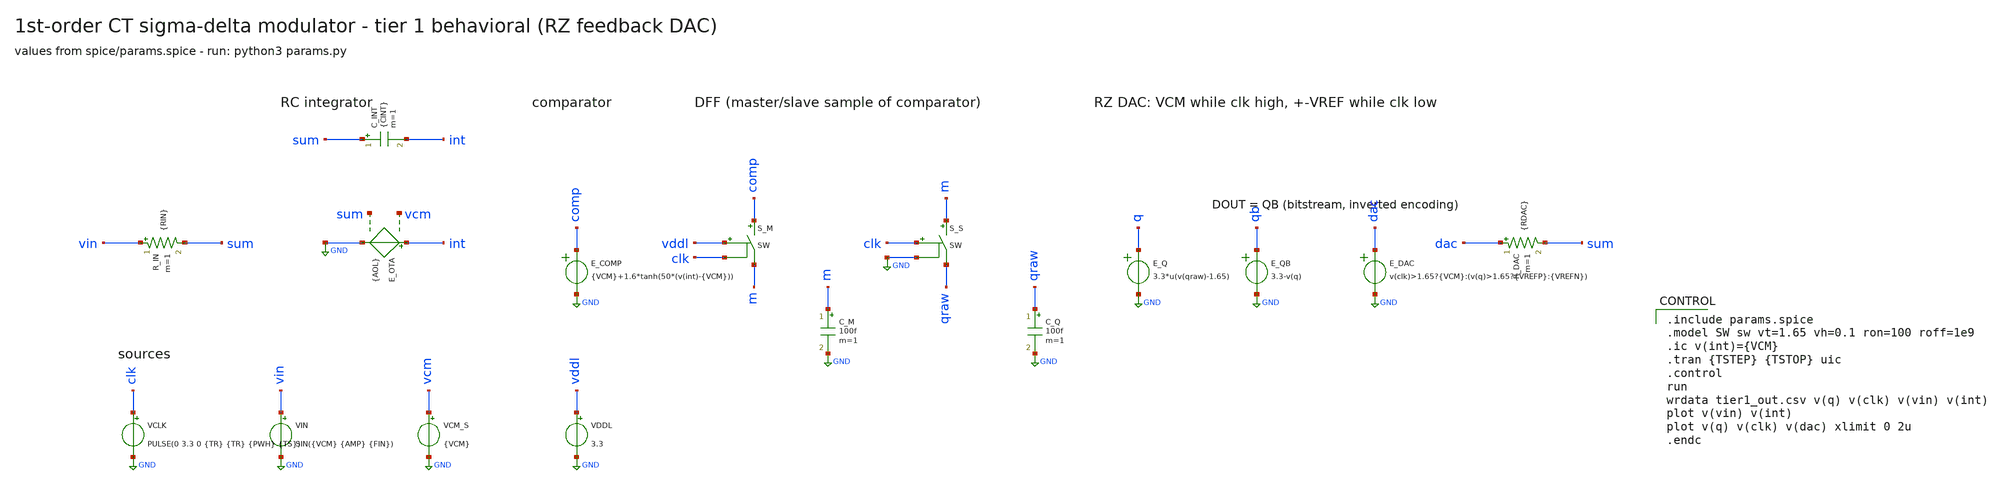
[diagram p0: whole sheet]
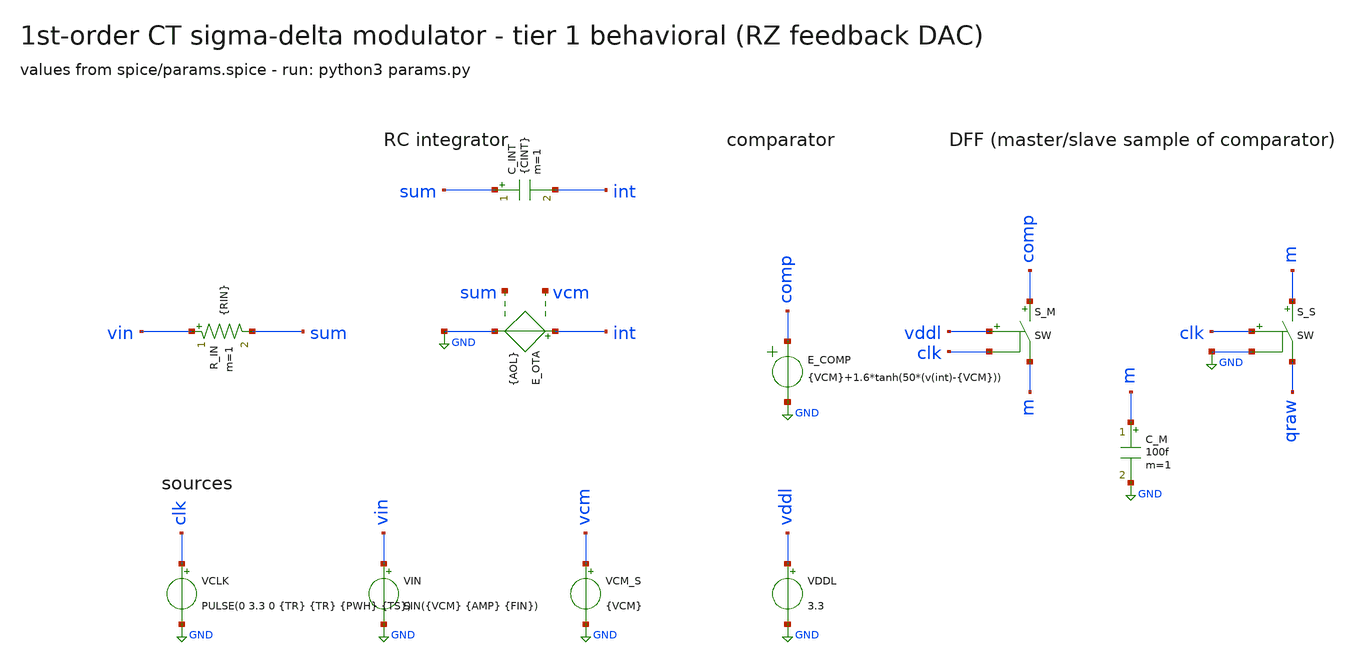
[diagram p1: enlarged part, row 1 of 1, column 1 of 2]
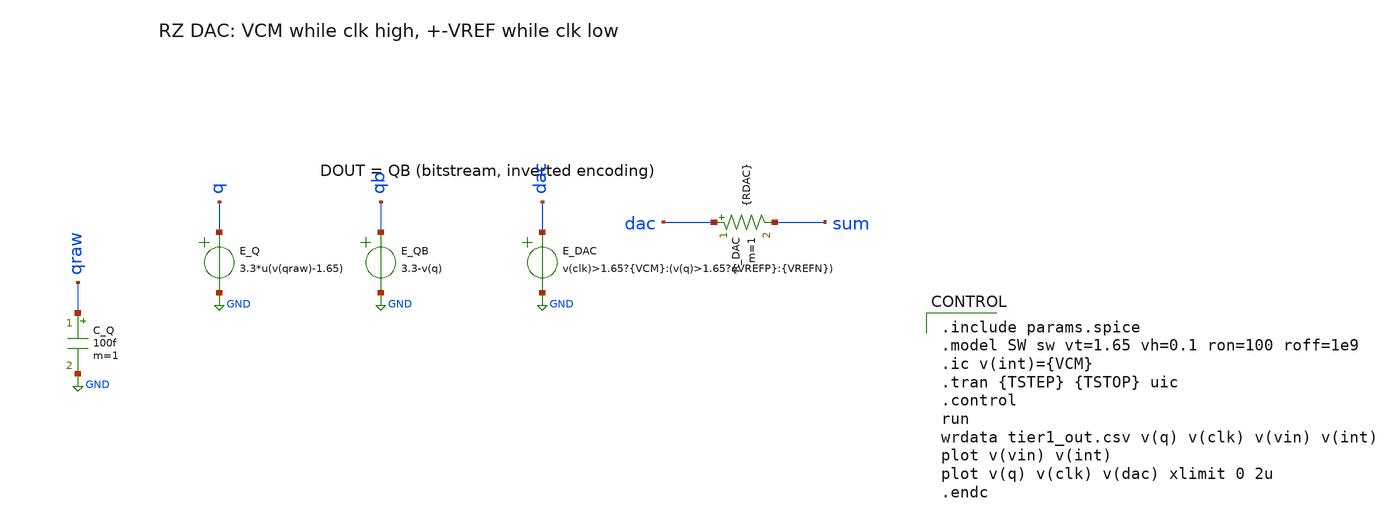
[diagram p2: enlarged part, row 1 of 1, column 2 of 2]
** sch_path: xschem/tier1_sdm.sch
**.subckt tier1_sdm
R_IN vin sum {RIN} m=1
C_INT sum int {CINT} m=1
E_OTA int GND vcm sum {AOL}
E_COMP comp GND VOL=' {VCM}+1.6*tanh(50*(v(int)-{VCM})) '
S_M comp m vddl clk SW
C_M m GND 100f m=1
S_S m qraw clk GND SW
C_Q qraw GND 100f m=1
E_Q q GND VOL=' 3.3*u(v(qraw)-1.65) '
E_QB qb GND VOL=' 3.3-v(q) '
E_DAC dac GND VOL=' v(clk)>1.65?{VCM}:(v(q)>1.65?{VREFP}:{VREFN}) '
R_DAC dac sum {RDAC} m=1
VCLK clk GND PULSE(0 3.3 0 {TR} {TR} {PWH} {TS})
VIN vin GND SIN({VCM} {AMP} {FIN})
VCM_S vcm GND {VCM}
VDDL vddl GND 3.3
**** begin user architecture code

.include params.spice
.model SW sw vt=1.65 vh=0.1 ron=100 roff=1e9
.ic v(int)={VCM}
.tran {TSTEP} {TSTOP} uic
.control
run
wrdata tier1_out.csv v(q) v(clk) v(vin) v(int)
plot v(vin) v(int)
plot v(q) v(clk) v(dac) xlimit 0 2u
.endc


**** end user architecture code
**.ends
.GLOBAL GND
.end
